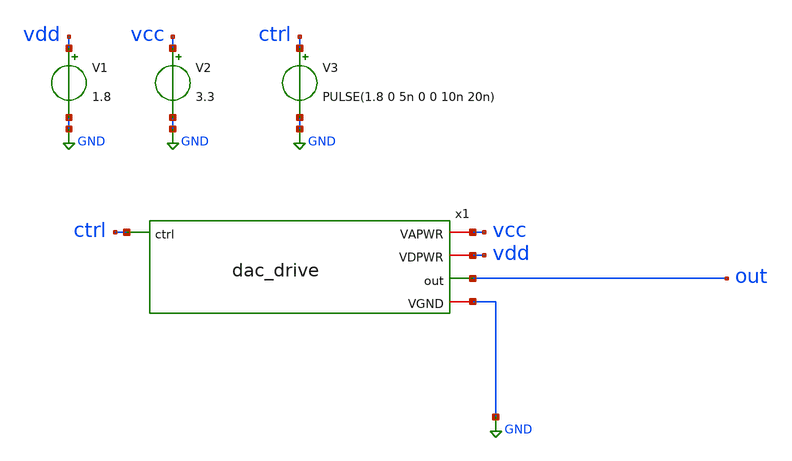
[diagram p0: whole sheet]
** sch_path: xschem/tb_dac_drive.sch
**.subckt tb_dac_drive
V2 vcc GND 3.3
V3 ctrl GND PULSE(1.8 0 5n 0 0 10n 20n)
V1 vdd GND 1.8
x1 vcc vdd ctrl out GND dac_drive
**** begin user architecture code

** opencircuitdesign pdks install
.lib $::SKYWATER_MODELS/sky130.lib.spice tt
.include $::SKYWATER_STDCELLS/sky130_fd_sc_hd.spice





.param mc_mm_switch=0
.control
tran 10p 100n
write tb_dac_drive.raw
*quit 0
.endc
.end


**** end user architecture code
**.ends

* expanding   symbol:  dac_drive.sym # of pins=5
** sym_path: xschem/dac_drive.sym
** sch_path: xschem/dac_drive.sch
.subckt dac_drive VAPWR VDPWR ctrl out VGND
*.ipin ctrl
*.iopin VGND
*.iopin VDPWR
*.iopin VAPWR
*.opin out
XM8 ctrl_n ctrl VDPWR VDPWR sky130_fd_pr__pfet_01v8_hvt L=0.15 W=1 nf=1 ad='int((nf+1)/2) * W/nf * 0.29'
+ as='int((nf+2)/2) * W/nf * 0.29' pd='2*int((nf+1)/2) * (W/nf + 0.29)' ps='2*int((nf+2)/2) * (W/nf + 0.29)'
+ nrd='0.29 / W' nrs='0.29 / W' sa=0 sb=0 sd=0 mult=1 m=1
XM7 ctrl_n ctrl VGND VGND sky130_fd_pr__nfet_01v8 L=0.15 W=0.42 nf=1 ad='int((nf+1)/2) * W/nf * 0.29'
+ as='int((nf+2)/2) * W/nf * 0.29' pd='2*int((nf+1)/2) * (W/nf + 0.29)' ps='2*int((nf+2)/2) * (W/nf + 0.29)'
+ nrd='0.29 / W' nrs='0.29 / W' sa=0 sb=0 sd=0 mult=1 m=1
XM11 m9m11 m10m12 VAPWR VAPWR sky130_fd_pr__pfet_g5v0d10v5 L=0.5 W=0.42 nf=1 ad='int((nf+1)/2) * W/nf * 0.29'
+ as='int((nf+2)/2) * W/nf * 0.29' pd='2*int((nf+1)/2) * (W/nf + 0.29)' ps='2*int((nf+2)/2) * (W/nf + 0.29)'
+ nrd='0.29 / W' nrs='0.29 / W' sa=0 sb=0 sd=0 mult=1 m=1
XM9 m9m11 ctrl VGND VGND sky130_fd_pr__nfet_g5v0d10v5 L=0.5 W=0.42 nf=1 ad='int((nf+1)/2) * W/nf * 0.29'
+ as='int((nf+2)/2) * W/nf * 0.29' pd='2*int((nf+1)/2) * (W/nf + 0.29)' ps='2*int((nf+2)/2) * (W/nf + 0.29)'
+ nrd='0.29 / W' nrs='0.29 / W' sa=0 sb=0 sd=0 mult=1 m=1
XM10 m10m12 ctrl_n VGND VGND sky130_fd_pr__nfet_g5v0d10v5 L=0.5 W=0.42 nf=1 ad='int((nf+1)/2) * W/nf * 0.29'
+ as='int((nf+2)/2) * W/nf * 0.29' pd='2*int((nf+1)/2) * (W/nf + 0.29)' ps='2*int((nf+2)/2) * (W/nf + 0.29)'
+ nrd='0.29 / W' nrs='0.29 / W' sa=0 sb=0 sd=0 mult=1 m=1
XM12 m10m12 m9m11 VAPWR VAPWR sky130_fd_pr__pfet_g5v0d10v5 L=0.5 W=0.42 nf=1 ad='int((nf+1)/2) * W/nf * 0.29'
+ as='int((nf+2)/2) * W/nf * 0.29' pd='2*int((nf+1)/2) * (W/nf + 0.29)' ps='2*int((nf+2)/2) * (W/nf + 0.29)'
+ nrd='0.29 / W' nrs='0.29 / W' sa=0 sb=0 sd=0 mult=1 m=1
XM1 out_drive m10m12 VAPWR VAPWR sky130_fd_pr__pfet_g5v0d10v5 L=0.5 W=0.84 nf=1 ad='int((nf+1)/2) * W/nf * 0.29'
+ as='int((nf+2)/2) * W/nf * 0.29' pd='2*int((nf+1)/2) * (W/nf + 0.29)' ps='2*int((nf+2)/2) * (W/nf + 0.29)'
+ nrd='0.29 / W' nrs='0.29 / W' sa=0 sb=0 sd=0 mult=1 m=1
XM2 out_drive m10m12 VGND VGND sky130_fd_pr__nfet_g5v0d10v5 L=0.5 W=0.42 nf=1 ad='int((nf+1)/2) * W/nf * 0.29'
+ as='int((nf+2)/2) * W/nf * 0.29' pd='2*int((nf+1)/2) * (W/nf + 0.29)' ps='2*int((nf+2)/2) * (W/nf + 0.29)'
+ nrd='0.29 / W' nrs='0.29 / W' sa=0 sb=0 sd=0 mult=1 m=1
XM3 out out_drive VAPWR VAPWR sky130_fd_pr__pfet_g5v0d10v5 L=0.5 W=9 nf=3 ad='int((nf+1)/2) * W/nf * 0.29'
+ as='int((nf+2)/2) * W/nf * 0.29' pd='2*int((nf+1)/2) * (W/nf + 0.29)' ps='2*int((nf+2)/2) * (W/nf + 0.29)'
+ nrd='0.29 / W' nrs='0.29 / W' sa=0 sb=0 sd=0 mult=1 m=1
XM4 out out_drive VGND VGND sky130_fd_pr__nfet_g5v0d10v5 L=0.5 W=3 nf=1 ad='int((nf+1)/2) * W/nf * 0.29'
+ as='int((nf+2)/2) * W/nf * 0.29' pd='2*int((nf+1)/2) * (W/nf + 0.29)' ps='2*int((nf+2)/2) * (W/nf + 0.29)'
+ nrd='0.29 / W' nrs='0.29 / W' sa=0 sb=0 sd=0 mult=1 m=1
.ends

.GLOBAL GND
.end
